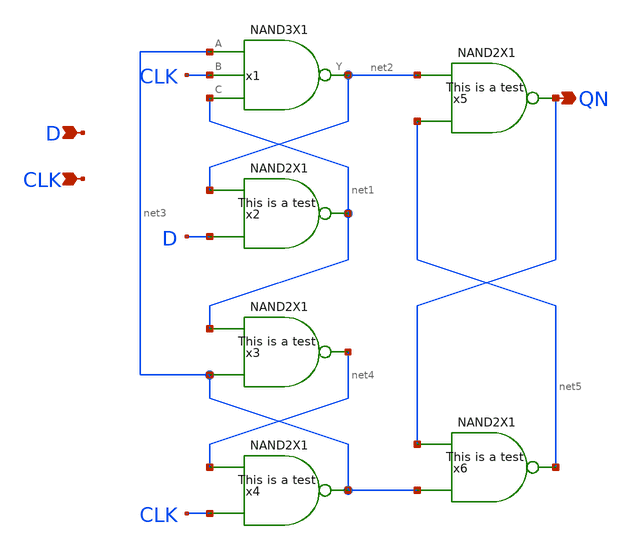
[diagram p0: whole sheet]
** sch_path: lib/xschem/DFFQNX1.sch
**.subckt DFFQNX1 QN D CLK
*.opin QN
*.ipin D
*.ipin CLK
x1 net2 net3 CLK net1 VDD VSS NAND3X1
x2 net1 net2 D VDD VSS NAND2X1
x3 net4 net1 net3 VDD VSS NAND2X1
x4 net3 net4 CLK VDD VSS NAND2X1
x5 QN net2 net5 VDD VSS NAND2X1
x6 net5 QN net3 VDD VSS NAND2X1
**.ends
.end
